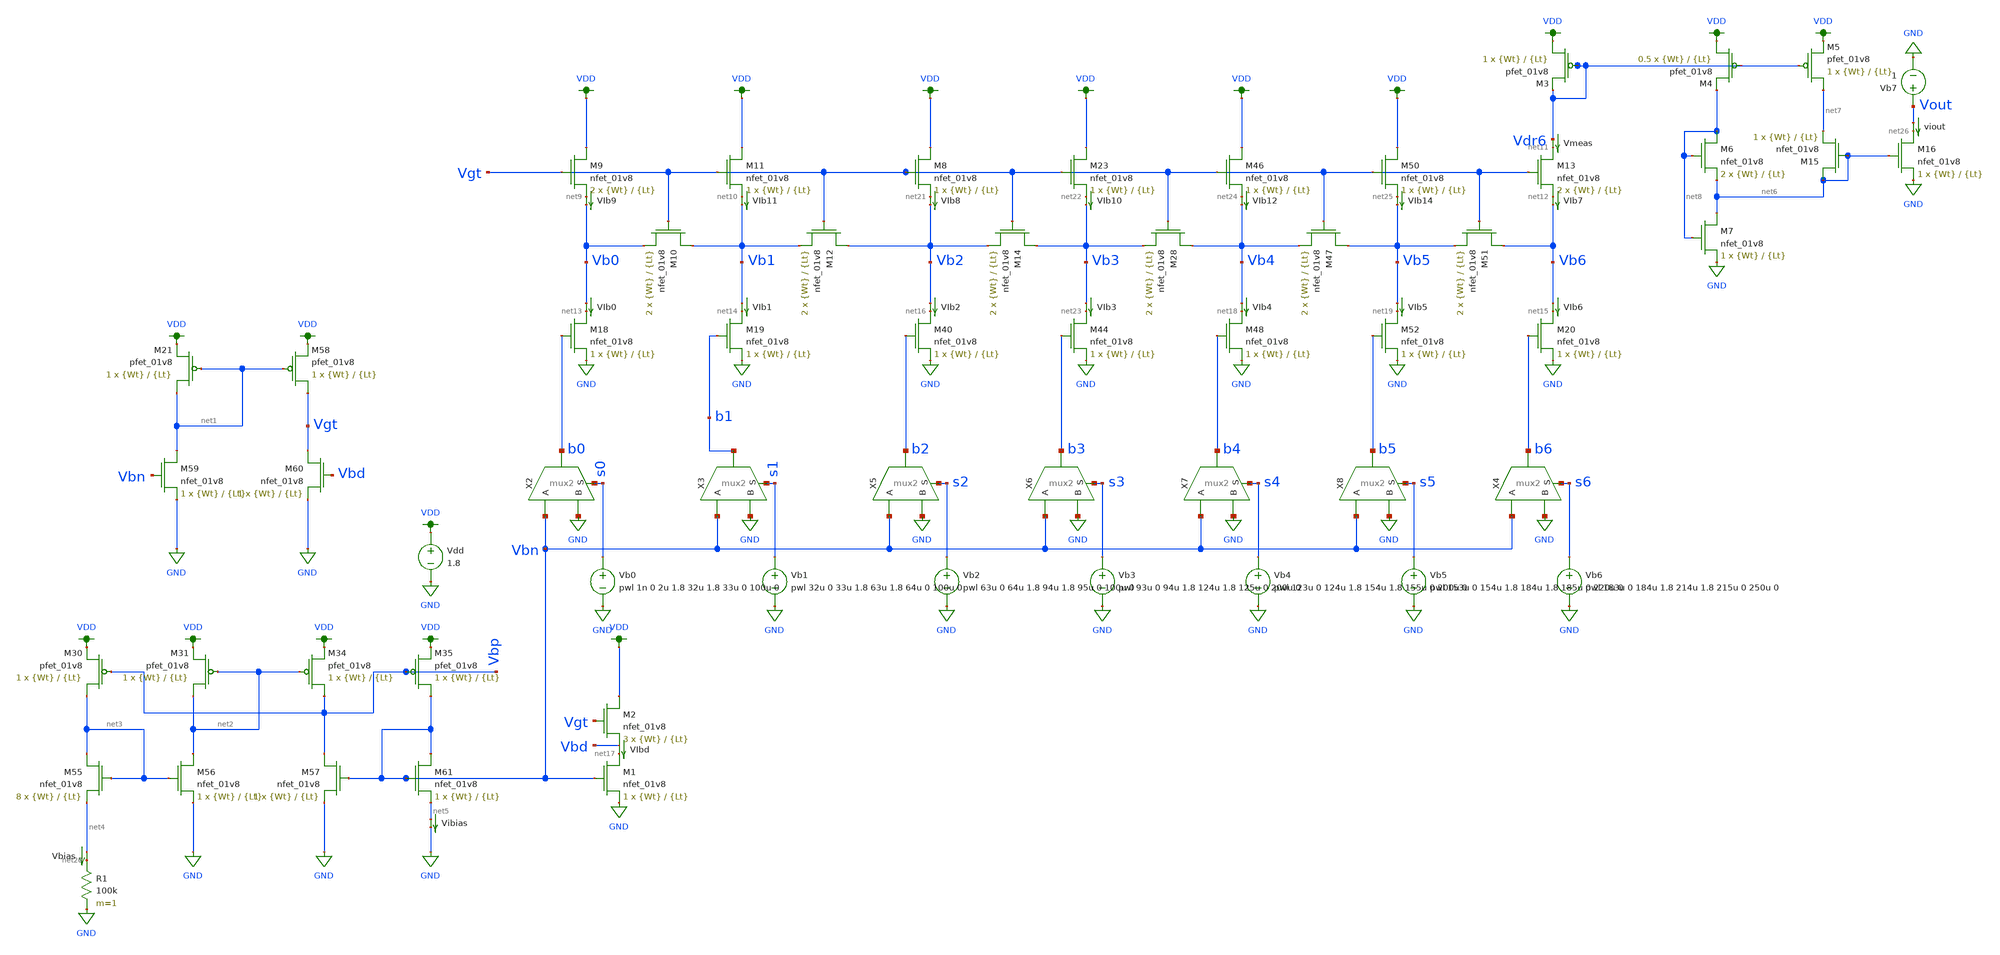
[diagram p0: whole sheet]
** sch_path: schematic/dac7_test_thomas_cascode_idnl.sch
**.subckt dac7_test_thomas_cascode_idnl
X2 b0 Vbn GND s0 mux2
X3 b1 Vbn GND s1 mux2
Vdd VDD GND 1.8
Vb0 s0 GND pwl 1n 0 2u 1.8 32u 1.8 33u 0 100u 0
Vb1 s1 GND pwl 32u 0 33u 1.8 63u 1.8 64u 0 100u 0
Vb2 s2 GND pwl 63u 0 64u 1.8 94u 1.8 95u 0 100u 0
XM9 VDD Vgt net9 GND sky130_fd_pr__nfet_01v8 L={Lt} W={Wt} nf=1 ad='int((nf+1)/2) * W/nf * 0.29' as='int((nf+2)/2) * W/nf * 0.29'
+ pd='2*int((nf+1)/2) * (W/nf + 0.29)' ps='2*int((nf+2)/2) * (W/nf + 0.29)' nrd='0.29 / W' nrs='0.29 / W'
+ sa=0 sb=0 sd=0 mult=2 m=2
XM10 Vb1 Vgt Vb0 GND sky130_fd_pr__nfet_01v8 L={Lt} W={Wt} nf=1 ad='int((nf+1)/2) * W/nf * 0.29' as='int((nf+2)/2) * W/nf * 0.29'
+ pd='2*int((nf+1)/2) * (W/nf + 0.29)' ps='2*int((nf+2)/2) * (W/nf + 0.29)' nrd='0.29 / W' nrs='0.29 / W'
+ sa=0 sb=0 sd=0 mult=2 m=2
XM11 VDD Vgt net10 GND sky130_fd_pr__nfet_01v8 L={Lt} W={Wt} nf=1 ad='int((nf+1)/2) * W/nf * 0.29' as='int((nf+2)/2) * W/nf * 0.29'
+ pd='2*int((nf+1)/2) * (W/nf + 0.29)' ps='2*int((nf+2)/2) * (W/nf + 0.29)' nrd='0.29 / W' nrs='0.29 / W'
+ sa=0 sb=0 sd=0 mult=1 m=1
XM12 Vb2 Vgt Vb1 GND sky130_fd_pr__nfet_01v8 L={Lt} W={Wt} nf=1 ad='int((nf+1)/2) * W/nf * 0.29' as='int((nf+2)/2) * W/nf * 0.29'
+ pd='2*int((nf+1)/2) * (W/nf + 0.29)' ps='2*int((nf+2)/2) * (W/nf + 0.29)' nrd='0.29 / W' nrs='0.29 / W'
+ sa=0 sb=0 sd=0 mult=2 m=2
XM13 net11 Vgt net12 GND sky130_fd_pr__nfet_01v8 L={Lt} W={Wt} nf=1 ad='int((nf+1)/2) * W/nf * 0.29'
+ as='int((nf+2)/2) * W/nf * 0.29' pd='2*int((nf+1)/2) * (W/nf + 0.29)' ps='2*int((nf+2)/2) * (W/nf + 0.29)'
+ nrd='0.29 / W' nrs='0.29 / W' sa=0 sb=0 sd=0 mult=2 m=2
XM18 net13 b0 GND GND sky130_fd_pr__nfet_01v8 L={Lt} W={Wt} nf=1 ad='int((nf+1)/2) * W/nf * 0.29' as='int((nf+2)/2) * W/nf * 0.29'
+ pd='2*int((nf+1)/2) * (W/nf + 0.29)' ps='2*int((nf+2)/2) * (W/nf + 0.29)' nrd='0.29 / W' nrs='0.29 / W'
+ sa=0 sb=0 sd=0 mult=1 m=1
XM19 net14 b1 GND GND sky130_fd_pr__nfet_01v8 L={Lt} W={Wt} nf=1 ad='int((nf+1)/2) * W/nf * 0.29' as='int((nf+2)/2) * W/nf * 0.29'
+ pd='2*int((nf+1)/2) * (W/nf + 0.29)' ps='2*int((nf+2)/2) * (W/nf + 0.29)' nrd='0.29 / W' nrs='0.29 / W'
+ sa=0 sb=0 sd=0 mult=1 m=1
XM20 net15 b6 GND GND sky130_fd_pr__nfet_01v8 L={Lt} W={Wt} nf=1 ad='int((nf+1)/2) * W/nf * 0.29' as='int((nf+2)/2) * W/nf * 0.29'
+ pd='2*int((nf+1)/2) * (W/nf + 0.29)' ps='2*int((nf+2)/2) * (W/nf + 0.29)' nrd='0.29 / W' nrs='0.29 / W'
+ sa=0 sb=0 sd=0 mult=1 m=1
Vmeas Vdr6 net11 0
.save i(vmeas)
VIb0 Vb0 net13 0
.save i(vib0)
VIb1 Vb1 net14 0
.save i(vib1)
VIb2 Vb2 net16 0
.save i(vib2)
XM1 net17 Vbn GND GND sky130_fd_pr__nfet_01v8 L={Lt} W={Wt} nf=1 ad='int((nf+1)/2) * W/nf * 0.29' as='int((nf+2)/2) * W/nf * 0.29'
+ pd='2*int((nf+1)/2) * (W/nf + 0.29)' ps='2*int((nf+2)/2) * (W/nf + 0.29)' nrd='0.29 / W' nrs='0.29 / W'
+ sa=0 sb=0 sd=0 mult=1 m=1
VIbd Vbd net17 0
.save i(vibd)
VIb4 Vb4 net18 0
.save i(vib4)
VIb5 Vb5 net19 0
.save i(vib5)
VIb6 Vb6 net15 0
.save i(vib6)
XM2 VDD Vgt Vbd GND sky130_fd_pr__nfet_01v8 L={Lt} W={Wt} nf=1 ad='int((nf+1)/2) * W/nf * 0.29' as='int((nf+2)/2) * W/nf * 0.29'
+ pd='2*int((nf+1)/2) * (W/nf + 0.29)' ps='2*int((nf+2)/2) * (W/nf + 0.29)' nrd='0.29 / W' nrs='0.29 / W'
+ sa=0 sb=0 sd=0 mult=3 m=3
XM21 net1 net1 VDD VDD sky130_fd_pr__pfet_01v8 L={Lt} W={Wt} nf=1 ad='int((nf+1)/2) * W/nf * 0.29' as='int((nf+2)/2) * W/nf * 0.29'
+ pd='2*int((nf+1)/2) * (W/nf + 0.29)' ps='2*int((nf+2)/2) * (W/nf + 0.29)' nrd='0.29 / W' nrs='0.29 / W'
+ sa=0 sb=0 sd=0 mult=1 m=1
XM58 Vgt net1 VDD VDD sky130_fd_pr__pfet_01v8 L={Lt} W={Wt} nf=1 ad='int((nf+1)/2) * W/nf * 0.29' as='int((nf+2)/2) * W/nf * 0.29'
+ pd='2*int((nf+1)/2) * (W/nf + 0.29)' ps='2*int((nf+2)/2) * (W/nf + 0.29)' nrd='0.29 / W' nrs='0.29 / W'
+ sa=0 sb=0 sd=0 mult=1 m=1
XM59 net1 Vbn GND GND sky130_fd_pr__nfet_01v8 L={Lt} W={Wt} nf=1 ad='int((nf+1)/2) * W/nf * 0.29' as='int((nf+2)/2) * W/nf * 0.29'
+ pd='2*int((nf+1)/2) * (W/nf + 0.29)' ps='2*int((nf+2)/2) * (W/nf + 0.29)' nrd='0.29 / W' nrs='0.29 / W'
+ sa=0 sb=0 sd=0 mult=1 m=1
XM60 Vgt Vbd GND GND sky130_fd_pr__nfet_01v8 L={Lt} W={Wt} nf=1 ad='int((nf+1)/2) * W/nf * 0.29' as='int((nf+2)/2) * W/nf * 0.29'
+ pd='2*int((nf+1)/2) * (W/nf + 0.29)' ps='2*int((nf+2)/2) * (W/nf + 0.29)' nrd='0.29 / W' nrs='0.29 / W'
+ sa=0 sb=0 sd=0 mult=1 m=1
R1 net20 GND 100k m=1
Vbias net4 net20 0
.save i(vbias)
X5 b2 Vbn GND s2 mux2
Vb3 s3 GND pwl 93u 0 94u 1.8 124u 1.8 125u 0 200u 0
XM8 VDD Vgt net21 GND sky130_fd_pr__nfet_01v8 L={Lt} W={Wt} nf=1 ad='int((nf+1)/2) * W/nf * 0.29' as='int((nf+2)/2) * W/nf * 0.29'
+ pd='2*int((nf+1)/2) * (W/nf + 0.29)' ps='2*int((nf+2)/2) * (W/nf + 0.29)' nrd='0.29 / W' nrs='0.29 / W'
+ sa=0 sb=0 sd=0 mult=1 m=1
XM14 Vb3 Vgt Vb2 GND sky130_fd_pr__nfet_01v8 L={Lt} W={Wt} nf=1 ad='int((nf+1)/2) * W/nf * 0.29' as='int((nf+2)/2) * W/nf * 0.29'
+ pd='2*int((nf+1)/2) * (W/nf + 0.29)' ps='2*int((nf+2)/2) * (W/nf + 0.29)' nrd='0.29 / W' nrs='0.29 / W'
+ sa=0 sb=0 sd=0 mult=2 m=2
XM40 net16 b2 GND GND sky130_fd_pr__nfet_01v8 L={Lt} W={Wt} nf=1 ad='int((nf+1)/2) * W/nf * 0.29' as='int((nf+2)/2) * W/nf * 0.29'
+ pd='2*int((nf+1)/2) * (W/nf + 0.29)' ps='2*int((nf+2)/2) * (W/nf + 0.29)' nrd='0.29 / W' nrs='0.29 / W'
+ sa=0 sb=0 sd=0 mult=1 m=1
VIb7 net12 Vb6 0
.save i(vib7)
VIb8 net21 Vb2 0
.save i(vib8)
X6 b3 Vbn GND s3 mux2
Vb4 s4 GND pwl 123u 0 124u 1.8 154u 1.8 155u 0 200u 0
XM23 VDD Vgt net22 GND sky130_fd_pr__nfet_01v8 L={Lt} W={Wt} nf=1 ad='int((nf+1)/2) * W/nf * 0.29' as='int((nf+2)/2) * W/nf * 0.29'
+ pd='2*int((nf+1)/2) * (W/nf + 0.29)' ps='2*int((nf+2)/2) * (W/nf + 0.29)' nrd='0.29 / W' nrs='0.29 / W'
+ sa=0 sb=0 sd=0 mult=1 m=1
XM28 Vb4 Vgt Vb3 GND sky130_fd_pr__nfet_01v8 L={Lt} W={Wt} nf=1 ad='int((nf+1)/2) * W/nf * 0.29' as='int((nf+2)/2) * W/nf * 0.29'
+ pd='2*int((nf+1)/2) * (W/nf + 0.29)' ps='2*int((nf+2)/2) * (W/nf + 0.29)' nrd='0.29 / W' nrs='0.29 / W'
+ sa=0 sb=0 sd=0 mult=2 m=2
XM44 net23 b3 GND GND sky130_fd_pr__nfet_01v8 L={Lt} W={Wt} nf=1 ad='int((nf+1)/2) * W/nf * 0.29' as='int((nf+2)/2) * W/nf * 0.29'
+ pd='2*int((nf+1)/2) * (W/nf + 0.29)' ps='2*int((nf+2)/2) * (W/nf + 0.29)' nrd='0.29 / W' nrs='0.29 / W'
+ sa=0 sb=0 sd=0 mult=1 m=1
VIb3 Vb3 net23 0
.save i(vib3)
VIb10 net22 Vb3 0
.save i(vib10)
X7 b4 Vbn GND s4 mux2
Vb5 s5 GND pwl 153u 0 154u 1.8 184u 1.8 185u 0 220u 0
XM46 VDD Vgt net24 GND sky130_fd_pr__nfet_01v8 L={Lt} W={Wt} nf=1 ad='int((nf+1)/2) * W/nf * 0.29' as='int((nf+2)/2) * W/nf * 0.29'
+ pd='2*int((nf+1)/2) * (W/nf + 0.29)' ps='2*int((nf+2)/2) * (W/nf + 0.29)' nrd='0.29 / W' nrs='0.29 / W'
+ sa=0 sb=0 sd=0 mult=1 m=1
XM47 Vb5 Vgt Vb4 GND sky130_fd_pr__nfet_01v8 L={Lt} W={Wt} nf=1 ad='int((nf+1)/2) * W/nf * 0.29' as='int((nf+2)/2) * W/nf * 0.29'
+ pd='2*int((nf+1)/2) * (W/nf + 0.29)' ps='2*int((nf+2)/2) * (W/nf + 0.29)' nrd='0.29 / W' nrs='0.29 / W'
+ sa=0 sb=0 sd=0 mult=2 m=2
XM48 net18 b4 GND GND sky130_fd_pr__nfet_01v8 L={Lt} W={Wt} nf=1 ad='int((nf+1)/2) * W/nf * 0.29' as='int((nf+2)/2) * W/nf * 0.29'
+ pd='2*int((nf+1)/2) * (W/nf + 0.29)' ps='2*int((nf+2)/2) * (W/nf + 0.29)' nrd='0.29 / W' nrs='0.29 / W'
+ sa=0 sb=0 sd=0 mult=1 m=1
VIb9 net9 Vb0 0
.save i(vib9)
VIb12 net24 Vb4 0
.save i(vib12)
X8 b5 Vbn GND s5 mux2
XM50 VDD Vgt net25 GND sky130_fd_pr__nfet_01v8 L={Lt} W={Wt} nf=1 ad='int((nf+1)/2) * W/nf * 0.29' as='int((nf+2)/2) * W/nf * 0.29'
+ pd='2*int((nf+1)/2) * (W/nf + 0.29)' ps='2*int((nf+2)/2) * (W/nf + 0.29)' nrd='0.29 / W' nrs='0.29 / W'
+ sa=0 sb=0 sd=0 mult=1 m=1
XM51 Vb6 Vgt Vb5 GND sky130_fd_pr__nfet_01v8 L={Lt} W={Wt} nf=1 ad='int((nf+1)/2) * W/nf * 0.29' as='int((nf+2)/2) * W/nf * 0.29'
+ pd='2*int((nf+1)/2) * (W/nf + 0.29)' ps='2*int((nf+2)/2) * (W/nf + 0.29)' nrd='0.29 / W' nrs='0.29 / W'
+ sa=0 sb=0 sd=0 mult=2 m=2
XM52 net19 b5 GND GND sky130_fd_pr__nfet_01v8 L={Lt} W={Wt} nf=1 ad='int((nf+1)/2) * W/nf * 0.29' as='int((nf+2)/2) * W/nf * 0.29'
+ pd='2*int((nf+1)/2) * (W/nf + 0.29)' ps='2*int((nf+2)/2) * (W/nf + 0.29)' nrd='0.29 / W' nrs='0.29 / W'
+ sa=0 sb=0 sd=0 mult=1 m=1
VIb11 net10 Vb1 0
.save i(vib11)
VIb14 net25 Vb5 0
.save i(vib14)
Vb6 s6 GND pwl 183u 0 184u 1.8 214u 1.8 215u 0 250u 0
X4 b6 Vbn GND s6 mux2
XM30 net3 Vbp VDD VDD sky130_fd_pr__pfet_01v8 L={Lt} W={Wt} nf=1 ad='int((nf+1)/2) * W/nf * 0.29' as='int((nf+2)/2) * W/nf * 0.29'
+ pd='2*int((nf+1)/2) * (W/nf + 0.29)' ps='2*int((nf+2)/2) * (W/nf + 0.29)' nrd='0.29 / W' nrs='0.29 / W'
+ sa=0 sb=0 sd=0 mult=1 m=1
XM31 net2 net2 VDD VDD sky130_fd_pr__pfet_01v8 L={Lt} W={Wt} nf=1 ad='int((nf+1)/2) * W/nf * 0.29' as='int((nf+2)/2) * W/nf * 0.29'
+ pd='2*int((nf+1)/2) * (W/nf + 0.29)' ps='2*int((nf+2)/2) * (W/nf + 0.29)' nrd='0.29 / W' nrs='0.29 / W'
+ sa=0 sb=0 sd=0 mult=1 m=1
XM34 Vbp net2 VDD VDD sky130_fd_pr__pfet_01v8 L={Lt} W={Wt} nf=1 ad='int((nf+1)/2) * W/nf * 0.29' as='int((nf+2)/2) * W/nf * 0.29'
+ pd='2*int((nf+1)/2) * (W/nf + 0.29)' ps='2*int((nf+2)/2) * (W/nf + 0.29)' nrd='0.29 / W' nrs='0.29 / W'
+ sa=0 sb=0 sd=0 mult=1 m=1
XM35 Vbn Vbp VDD VDD sky130_fd_pr__pfet_01v8 L={Lt} W={Wt} nf=1 ad='int((nf+1)/2) * W/nf * 0.29' as='int((nf+2)/2) * W/nf * 0.29'
+ pd='2*int((nf+1)/2) * (W/nf + 0.29)' ps='2*int((nf+2)/2) * (W/nf + 0.29)' nrd='0.29 / W' nrs='0.29 / W'
+ sa=0 sb=0 sd=0 mult=1 m=1
XM55 net3 net3 net4 GND sky130_fd_pr__nfet_01v8 L={Lt} W={Wt} nf=1 ad='int((nf+1)/2) * W/nf * 0.29' as='int((nf+2)/2) * W/nf * 0.29'
+ pd='2*int((nf+1)/2) * (W/nf + 0.29)' ps='2*int((nf+2)/2) * (W/nf + 0.29)' nrd='0.29 / W' nrs='0.29 / W'
+ sa=0 sb=0 sd=0 mult=8 m=8
XM56 net2 net3 GND GND sky130_fd_pr__nfet_01v8 L={Lt} W={Wt} nf=1 ad='int((nf+1)/2) * W/nf * 0.29' as='int((nf+2)/2) * W/nf * 0.29'
+ pd='2*int((nf+1)/2) * (W/nf + 0.29)' ps='2*int((nf+2)/2) * (W/nf + 0.29)' nrd='0.29 / W' nrs='0.29 / W'
+ sa=0 sb=0 sd=0 mult=1 m=1
XM57 Vbp Vbn GND GND sky130_fd_pr__nfet_01v8 L={Lt} W={Wt} nf=1 ad='int((nf+1)/2) * W/nf * 0.29' as='int((nf+2)/2) * W/nf * 0.29'
+ pd='2*int((nf+1)/2) * (W/nf + 0.29)' ps='2*int((nf+2)/2) * (W/nf + 0.29)' nrd='0.29 / W' nrs='0.29 / W'
+ sa=0 sb=0 sd=0 mult=1 m=1
XM61 Vbn Vbn net5 GND sky130_fd_pr__nfet_01v8 L={Lt} W={Wt} nf=1 ad='int((nf+1)/2) * W/nf * 0.29' as='int((nf+2)/2) * W/nf * 0.29'
+ pd='2*int((nf+1)/2) * (W/nf + 0.29)' ps='2*int((nf+2)/2) * (W/nf + 0.29)' nrd='0.29 / W' nrs='0.29 / W'
+ sa=0 sb=0 sd=0 mult=1 m=1
Vibias net5 GND 0
.save i(vibias)
XM3 VDD Vdr6 Vdr6 VDD sky130_fd_pr__pfet_01v8 L={Lt} W={Wt} nf=1 ad='int((nf+1)/2) * W/nf * 0.29' as='int((nf+2)/2) * W/nf * 0.29'
+ pd='2*int((nf+1)/2) * (W/nf + 0.29)' ps='2*int((nf+2)/2) * (W/nf + 0.29)' nrd='0.29 / W' nrs='0.29 / W'
+ sa=0 sb=0 sd=0 mult=1 m=1
XM4 VDD Vdr6 net8 VDD sky130_fd_pr__pfet_01v8 L={Lt} W={Wt} nf=1 ad='int((nf+1)/2) * W/nf * 0.29' as='int((nf+2)/2) * W/nf * 0.29'
+ pd='2*int((nf+1)/2) * (W/nf + 0.29)' ps='2*int((nf+2)/2) * (W/nf + 0.29)' nrd='0.29 / W' nrs='0.29 / W'
+ sa=0 sb=0 sd=0 mult=0.5 m=0.5
XM5 net7 Vdr6 VDD VDD sky130_fd_pr__pfet_01v8 L={Lt} W={Wt} nf=1 ad='int((nf+1)/2) * W/nf * 0.29' as='int((nf+2)/2) * W/nf * 0.29'
+ pd='2*int((nf+1)/2) * (W/nf + 0.29)' ps='2*int((nf+2)/2) * (W/nf + 0.29)' nrd='0.29 / W' nrs='0.29 / W'
+ sa=0 sb=0 sd=0 mult=1 m=1
XM6 net8 net8 net6 GND sky130_fd_pr__nfet_01v8 L={Lt} W={Wt} nf=1 ad='int((nf+1)/2) * W/nf * 0.29' as='int((nf+2)/2) * W/nf * 0.29'
+ pd='2*int((nf+1)/2) * (W/nf + 0.29)' ps='2*int((nf+2)/2) * (W/nf + 0.29)' nrd='0.29 / W' nrs='0.29 / W'
+ sa=0 sb=0 sd=0 mult=2 m=2
XM7 net6 net8 GND GND sky130_fd_pr__nfet_01v8 L={Lt} W={Wt} nf=1 ad='int((nf+1)/2) * W/nf * 0.29' as='int((nf+2)/2) * W/nf * 0.29'
+ pd='2*int((nf+1)/2) * (W/nf + 0.29)' ps='2*int((nf+2)/2) * (W/nf + 0.29)' nrd='0.29 / W' nrs='0.29 / W'
+ sa=0 sb=0 sd=0 mult=1 m=1
XM15 net6 net6 net7 GND sky130_fd_pr__nfet_01v8 L={Lt} W={Wt} nf=1 ad='int((nf+1)/2) * W/nf * 0.29' as='int((nf+2)/2) * W/nf * 0.29'
+ pd='2*int((nf+1)/2) * (W/nf + 0.29)' ps='2*int((nf+2)/2) * (W/nf + 0.29)' nrd='0.29 / W' nrs='0.29 / W'
+ sa=0 sb=0 sd=0 mult=1 m=1
XM16 net26 net6 GND GND sky130_fd_pr__nfet_01v8 L={Lt} W={Wt} nf=1 ad='int((nf+1)/2) * W/nf * 0.29' as='int((nf+2)/2) * W/nf * 0.29'
+ pd='2*int((nf+1)/2) * (W/nf + 0.29)' ps='2*int((nf+2)/2) * (W/nf + 0.29)' nrd='0.29 / W' nrs='0.29 / W'
+ sa=0 sb=0 sd=0 mult=1 m=1
Vb7 Vout GND 1
viout Vout net26 0
.save i(viout)
**** begin user architecture code

.option wnflag=1
.param MC_SWITCH=1.0
.lib ~/skywater/skywater-pdk/libraries/sky130_fd_pr_ngspice/latest/models/sky130.lib.spice tt


.param Wt = 20
.param Lt = 4
.control
*** change W and L for the next two lines as well !***
  let myW = 20
  let myL = 4
  set wr_singlescale
  let runs = 10
  let run = 1
  while run <= runs
    set appendwrite = FALSE
    set wr_vecnames
    let code = 0
    while code < 64
      if code eq 0
        let b0 = 0
      else
        let b0 = (code % 2) * 1.8
      end
      if floor(code / 2) eq 0
        let b1 = 0
      else
        let b1 = (floor(code / 2) % 2) * 1.8
      end
      if floor(code / 4) eq 0
        let b2 = 0
      else
        let b2 = (floor(code / 4) % 2) * 1.8
      end
      if floor(code / 8) eq 0
        let b3 = 0
      else
        let b3 = floor(code / 8) % 2 * 1.8
      end
      if floor(code / 16) eq 0
        let b4 = 0
      else
        let b4 = floor(code / 16) % 2 * 1.8
      end
      if floor(code / 32) eq 0
        let b5 = 0
      else
        let b5 = floor(code / 32) % 2 * 1.8
      end
      if floor(code / 64) eq 0
        let b6 = 0
      else
        let b6 = floor(code / 64) % 2 * 1.8
      end
      alter vb0 $&b0
      alter vb1 $&b1
      alter vb2 $&b2
      alter vb3 $&b3
      alter vb4 $&b4
      alter vb5 $&b5
      alter vb6 $&b6
      save v(b0) v(b1) v(b2) v(b3) v(b4) v(b5) v(b6) i(vbias) i(viout) v(vout)
      op
      wrdata ~/Documents/MADVLSI-MP4/schematic/data/dac7mc_L{$&myL}W{$&myW}op-{$&run}.txt v(b0) v(b1)
+ v(b2) v(b3) v(b4) v(b5) v(b6) i(vbias) i(viout) v(vout)
      if code eq 0
        set appendwrite
        set wr_vecnames = FALSE
      end
      let code = code + 1
    end
    reset
    let run = run + 1
  end

  set appendwrite = FALSE
  reset
  set wr_singlescale
  set wr_vecnames
  alter vb0 1.8
  alter vb1 1.8
  alter vb2 1.8
  alter vb3 1.8
  alter vb4 1.8
  alter vb5 1.8
  alter vb6 1.8
  save v(b0) v(b1) v(b2) v(b3) v(b4) v(b5) v(b6) i(vbias) i(viout) v(vout)
  dc Voutt 0 1.8 0.01
  run
  wrdata ~/Documents/MADVLSI-MP4/schematic/data/dac7mc_L{$&myL}W{$&myW}vout-1.txt v(b0) v(b1) v(b2) v(b3)
+ v(b4) v(b5) v(b6) i(vbias) i(viout) v(vout)

  reset
  set wr_singlescale
  set wr_vecnames
  alter vb0 1.8
  alter vb1 1.8
  alter vb2 1.8
  alter vb3 1.8
  alter vb4 1.8
  alter vb5 1.8
  alter vb6 0
  save v(b0) v(b1) v(b2) v(b3) v(b4) v(b5) v(b6) i(vbias) i(viout) v(vout)
  dc Voutt 0 1.8 0.01
  run
  wrdata ~/Documents/MADVLSI-MP4/schematic/data/dac7mc_L{$&myL}W{$&myW}vout-2.txt v(b0) v(b1) v(b2) v(b3)
+ v(b4) v(b5) v(b6) i(vbias) i(viout) v(vout)

  reset
  set wr_singlescale
  set wr_vecnames
  alter vb0 1.8
  alter vb1 1.8
  alter vb2 1.8
  alter vb3 1.8
  alter vb4 1.8
  alter vb5 1.8
  alter vb6 1.8
  save v(b0) v(b1) v(b2) v(b3) v(b4) v(b5) v(b6) i(vbias) i(viout) v(vout)
  dc Vdd 0 1.8 0.01
  run
  wrdata ~/Documents/MADVLSI-MP4/schematic/data/dac7mc_L{$&myL}W{$&myW}vdd-1.txt v(b0) v(b1) v(b2) v(b3)
+ v(b4) v(b5) v(b6) i(vbias) i(viout) v(vout)

  reset
  set wr_singlescale
  set wr_vecnames
  alter vb0 1.8
  alter vb1 1.8
  alter vb2 1.8
  alter vb3 1.8
  alter vb4 1.8
  alter vb5 1.8
  alter vb6 0
  save v(b0) v(b1) v(b2) v(b3) v(b4) v(b5) v(b6) i(vbias) i(viout) v(vout)
  dc Vdd 0 1.8 0.01
  run
  wrdata ~/Documents/MADVLSI-MP4/schematic/data/dac7mc_L{$&myL}W{$&myW}vdd-2.txt v(b0) v(b1) v(b2) v(b3)
+ v(b4) v(b5) v(b6) i(vbias) i(viout) v(vout)
.endc

**** end user architecture code
**.ends
.GLOBAL GND
.GLOBAL VDD
.end
